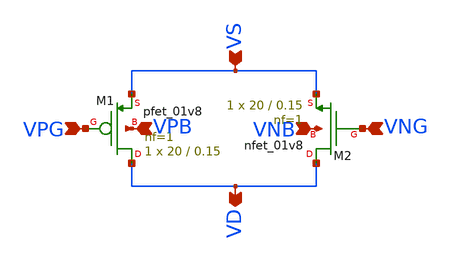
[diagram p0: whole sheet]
** sch_path: analog_mux_files 2/a_mux_switch.sch
**.subckt a_mux_switch VPG VNG VS VD VPB VNB
*.ipin VPG
*.ipin VNG
*.ipin VS
*.opin VD
*.ipin VPB
*.ipin VNB
XM1 VD VPG VS VPB sky130_fd_pr__pfet_01v8 L=0.15 W=20 nf=1 ad='int((nf+1)/2) * W/nf * 0.29' as='int((nf+2)/2) * W/nf * 0.29'
+ pd='2*int((nf+1)/2) * (W/nf + 0.29)' ps='2*int((nf+2)/2) * (W/nf + 0.29)' nrd='0.29 / W' nrs='0.29 / W'
+ sa=0 sb=0 sd=0 mult=1 m=1
XM2 VD VNG VS VNB sky130_fd_pr__nfet_01v8 L=0.15 W=20 nf=1 ad='int((nf+1)/2) * W/nf * 0.29' as='int((nf+2)/2) * W/nf * 0.29'
+ pd='2*int((nf+1)/2) * (W/nf + 0.29)' ps='2*int((nf+2)/2) * (W/nf + 0.29)' nrd='0.29 / W' nrs='0.29 / W'
+ sa=0 sb=0 sd=0 mult=1 m=1
**.ends
.end
